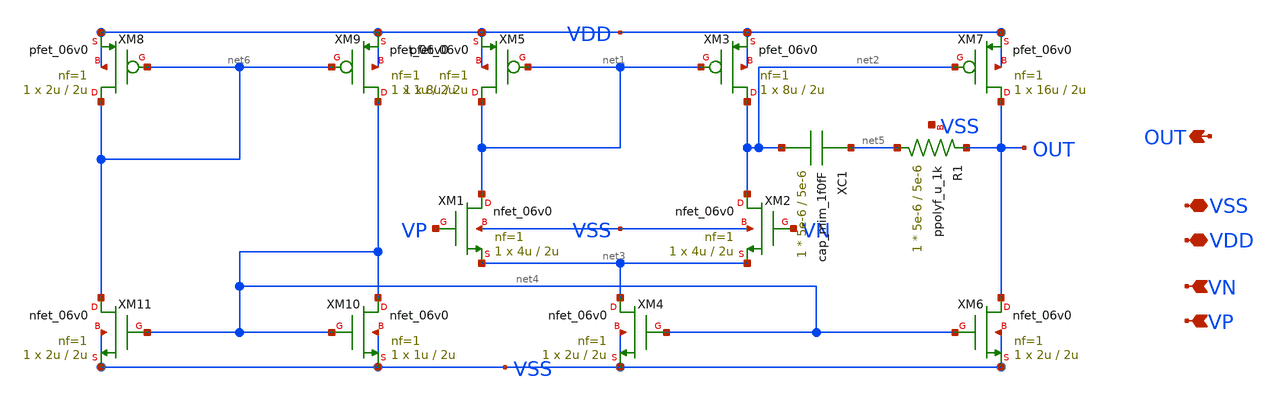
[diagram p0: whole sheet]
** sch_path: designs/libs/core_n-ota/n-ota-6v/n-ota-6v.sch
**.subckt n-ota-6v VN VP OUT VDD VSS
*.ipin VN
*.ipin VP
*.opin OUT
*.iopin VDD
*.iopin VSS
XM1 net1 VP net3 VSS nfet_06v0 L=2u W=4u nf=1 ad='int((nf+1)/2) * W/nf * 0.18u' as='int((nf+2)/2) * W/nf * 0.18u'
+ pd='2*int((nf+1)/2) * (W/nf + 0.18u)' ps='2*int((nf+2)/2) * (W/nf + 0.18u)' nrd='0.18u / W' nrs='0.18u / W'
+ sa=0 sb=0 sd=0 m=1
XM2 net2 VN net3 VSS nfet_06v0 L=2u W=4u nf=1 ad='int((nf+1)/2) * W/nf * 0.18u' as='int((nf+2)/2) * W/nf * 0.18u'
+ pd='2*int((nf+1)/2) * (W/nf + 0.18u)' ps='2*int((nf+2)/2) * (W/nf + 0.18u)' nrd='0.18u / W' nrs='0.18u / W'
+ sa=0 sb=0 sd=0 m=1
XM4 net3 net4 VSS VSS nfet_06v0 L=2u W=2u nf=1 ad='int((nf+1)/2) * W/nf * 0.18u' as='int((nf+2)/2) * W/nf * 0.18u'
+ pd='2*int((nf+1)/2) * (W/nf + 0.18u)' ps='2*int((nf+2)/2) * (W/nf + 0.18u)' nrd='0.18u / W' nrs='0.18u / W'
+ sa=0 sb=0 sd=0 m=1
XM3 net2 net1 VDD VDD pfet_06v0 L=2u W=8u nf=1 ad='int((nf+1)/2) * W/nf * 0.18u' as='int((nf+2)/2) * W/nf * 0.18u'
+ pd='2*int((nf+1)/2) * (W/nf + 0.18u)' ps='2*int((nf+2)/2) * (W/nf + 0.18u)' nrd='0.18u / W' nrs='0.18u / W'
+ sa=0 sb=0 sd=0 m=1
XM5 net1 net1 VDD VDD pfet_06v0 L=2u W=8u nf=1 ad='int((nf+1)/2) * W/nf * 0.18u' as='int((nf+2)/2) * W/nf * 0.18u'
+ pd='2*int((nf+1)/2) * (W/nf + 0.18u)' ps='2*int((nf+2)/2) * (W/nf + 0.18u)' nrd='0.18u / W' nrs='0.18u / W'
+ sa=0 sb=0 sd=0 m=1
XM6 OUT net4 VSS VSS nfet_06v0 L=2u W=2u nf=1 ad='int((nf+1)/2) * W/nf * 0.18u' as='int((nf+2)/2) * W/nf * 0.18u'
+ pd='2*int((nf+1)/2) * (W/nf + 0.18u)' ps='2*int((nf+2)/2) * (W/nf + 0.18u)' nrd='0.18u / W' nrs='0.18u / W'
+ sa=0 sb=0 sd=0 m=1
XM7 OUT net2 VDD VDD pfet_06v0 L=2u W=16u nf=1 ad='int((nf+1)/2) * W/nf * 0.18u' as='int((nf+2)/2) * W/nf * 0.18u'
+ pd='2*int((nf+1)/2) * (W/nf + 0.18u)' ps='2*int((nf+2)/2) * (W/nf + 0.18u)' nrd='0.18u / W' nrs='0.18u / W'
+ sa=0 sb=0 sd=0 m=1
XC1 net5 net2 cap_mim_1f0fF c_width=5e-6 c_length=5e-6 m=1
XR1 net5 OUT VSS ppolyf_u_1k r_width=5e-6 r_length=5e-6 m=1
XM8 net6 net6 VDD VDD pfet_06v0 L=2u W=2u nf=1 ad='int((nf+1)/2) * W/nf * 0.18u' as='int((nf+2)/2) * W/nf * 0.18u'
+ pd='2*int((nf+1)/2) * (W/nf + 0.18u)' ps='2*int((nf+2)/2) * (W/nf + 0.18u)' nrd='0.18u / W' nrs='0.18u / W'
+ sa=0 sb=0 sd=0 m=1
XM9 net4 net6 VDD VDD pfet_06v0 L=2u W=1u nf=1 ad='int((nf+1)/2) * W/nf * 0.18u' as='int((nf+2)/2) * W/nf * 0.18u'
+ pd='2*int((nf+1)/2) * (W/nf + 0.18u)' ps='2*int((nf+2)/2) * (W/nf + 0.18u)' nrd='0.18u / W' nrs='0.18u / W'
+ sa=0 sb=0 sd=0 m=1
XM10 net4 net4 VSS VSS nfet_06v0 L=2u W=1u nf=1 ad='int((nf+1)/2) * W/nf * 0.18u' as='int((nf+2)/2) * W/nf * 0.18u'
+ pd='2*int((nf+1)/2) * (W/nf + 0.18u)' ps='2*int((nf+2)/2) * (W/nf + 0.18u)' nrd='0.18u / W' nrs='0.18u / W'
+ sa=0 sb=0 sd=0 m=1
XM11 net6 net4 VSS VSS nfet_06v0 L=2u W=2u nf=1 ad='int((nf+1)/2) * W/nf * 0.18u' as='int((nf+2)/2) * W/nf * 0.18u'
+ pd='2*int((nf+1)/2) * (W/nf + 0.18u)' ps='2*int((nf+2)/2) * (W/nf + 0.18u)' nrd='0.18u / W' nrs='0.18u / W'
+ sa=0 sb=0 sd=0 m=1
**.ends
.end
